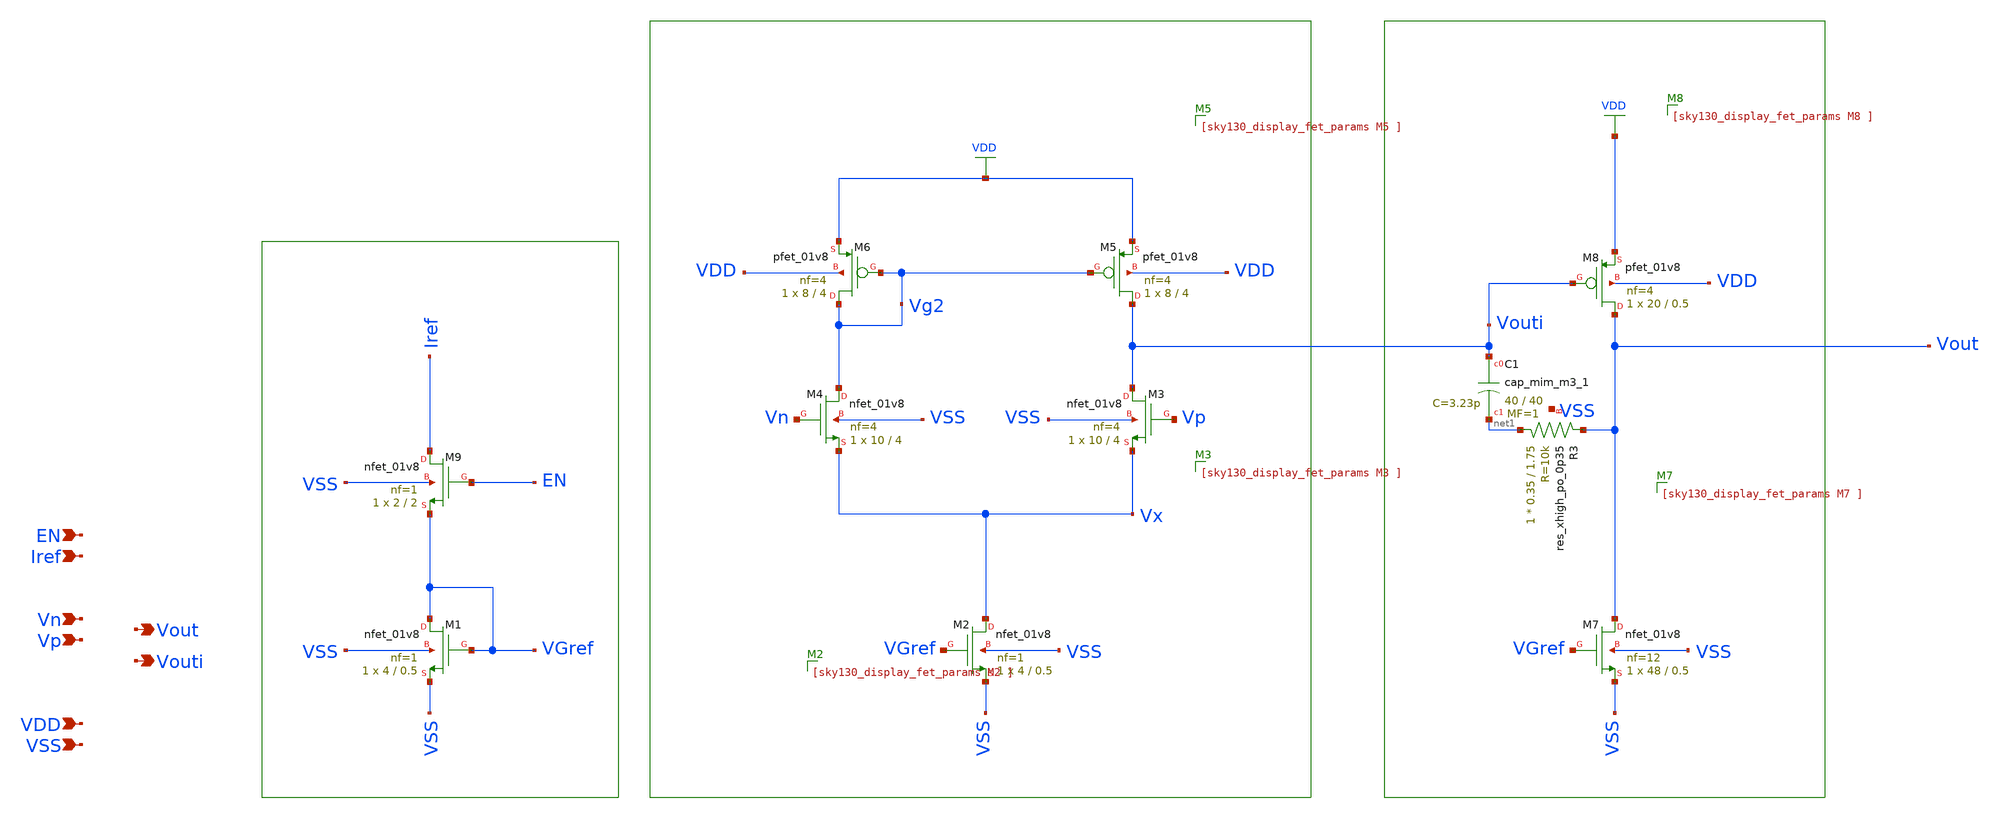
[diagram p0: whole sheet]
** sch_path: xschem/opamp.sch
**.subckt opamp VSS Vp Vout Vn VDD Iref Vouti EN
*.ipin VSS
*.ipin Vp
*.opin Vout
*.ipin Vn
*.ipin VDD
*.ipin Iref
*.opin Vouti
*.ipin EN
XM1 VGref VGref VSS VSS sky130_fd_pr__nfet_01v8 L=0.5 W=4 nf=1 ad='int((1 + 1)/2) * 4 / 1 * 0.29' as='int((1 + 2)/2) * 4 / 1 * 0.29'
+ pd='2*int((1 + 1)/2) * (4 / 1 + 0.29)' ps='2*int((1 + 2)/2) * (4 / 1 + 0.29)' nrd='0.29 / 4 ' nrs='0.29 / 4 '
+ sa=0 sb=0 sd=0 mult=1 m=1
XM2 Vx VGref VSS VSS sky130_fd_pr__nfet_01v8 L=0.5 W=4 nf=1 ad='int((1 + 1)/2) * 4 / 1 * 0.29' as='int((1 + 2)/2) * 4 / 1 * 0.29'
+ pd='2*int((1 + 1)/2) * (4 / 1 + 0.29)' ps='2*int((1 + 2)/2) * (4 / 1 + 0.29)' nrd='0.29 / 4 ' nrs='0.29 / 4 '
+ sa=0 sb=0 sd=0 mult=1 m=1
XM3 Vouti Vp Vx VSS sky130_fd_pr__nfet_01v8 L=4 W=10 nf=4 ad='int((4 + 1)/2) * 10 / 4 * 0.29' as='int((4 + 2)/2) * 10 / 4 * 0.29'
+ pd='2*int((4 + 1)/2) * (10 / 4 + 0.29)' ps='2*int((4 + 2)/2) * (10 / 4 + 0.29)' nrd='0.29 / 10 ' nrs='0.29 / 10 '
+ sa=0 sb=0 sd=0 mult=1 m=1
XM4 Vg2 Vn Vx VSS sky130_fd_pr__nfet_01v8 L=4 W=10 nf=4 ad='int((4 + 1)/2) * 10 / 4 * 0.29' as='int((4 + 2)/2) * 10 / 4 * 0.29'
+ pd='2*int((4 + 1)/2) * (10 / 4 + 0.29)' ps='2*int((4 + 2)/2) * (10 / 4 + 0.29)' nrd='0.29 / 10 ' nrs='0.29 / 10 '
+ sa=0 sb=0 sd=0 mult=1 m=1
XM5 Vouti Vg2 VDD VDD sky130_fd_pr__pfet_01v8 L=4 W=8 nf=4 ad='int((4 + 1)/2) * 8 / 4 * 0.29' as='int((4 + 2)/2) * 8 / 4 * 0.29'
+ pd='2*int((4 + 1)/2) * (8 / 4 + 0.29)' ps='2*int((4 + 2)/2) * (8 / 4 + 0.29)' nrd='0.29 / 8 ' nrs='0.29 / 8 '
+ sa=0 sb=0 sd=0 mult=1 m=1
XM6 Vg2 Vg2 VDD VDD sky130_fd_pr__pfet_01v8 L=4 W=8 nf=4 ad='int((4 + 1)/2) * 8 / 4 * 0.29' as='int((4 + 2)/2) * 8 / 4 * 0.29'
+ pd='2*int((4 + 1)/2) * (8 / 4 + 0.29)' ps='2*int((4 + 2)/2) * (8 / 4 + 0.29)' nrd='0.29 / 8 ' nrs='0.29 / 8 '
+ sa=0 sb=0 sd=0 mult=1 m=1
XM7 Vout VGref VSS VSS sky130_fd_pr__nfet_01v8 L=0.5 W=48 nf=12 ad='int((12 + 1)/2) * 48 / 12 * 0.29'
+ as='int((12 + 2)/2) * 48 / 12 * 0.29' pd='2*int((12 + 1)/2) * (48 / 12 + 0.29)' ps='2*int((12 + 2)/2) * (48 / 12 + 0.29)'
+ nrd='0.29 / 48 ' nrs='0.29 / 48 ' sa=0 sb=0 sd=0 mult=1 m=1
XM8 Vout Vouti VDD VDD sky130_fd_pr__pfet_01v8 L=0.5 W=20 nf=4 ad='int((4 + 1)/2) * 20 / 4 * 0.29' as='int((4 + 2)/2) * 20 / 4 * 0.29'
+ pd='2*int((4 + 1)/2) * (20 / 4 + 0.29)' ps='2*int((4 + 2)/2) * (20 / 4 + 0.29)' nrd='0.29 / 20 ' nrs='0.29 / 20 '
+ sa=0 sb=0 sd=0 mult=1 m=1
XM9 Iref EN VGref VSS sky130_fd_pr__nfet_01v8 L=2 W=2 nf=1 ad='int((1 + 1)/2) * 2 / 1 * 0.29' as='int((1 + 2)/2) * 2 / 1 * 0.29'
+ pd='2*int((1 + 1)/2) * (2 / 1 + 0.29)' ps='2*int((1 + 2)/2) * (2 / 1 + 0.29)' nrd='0.29 / 2 ' nrs='0.29 / 2 '
+ sa=0 sb=0 sd=0 mult=1 m=1
XC1 Vouti net1 sky130_fd_pr__cap_mim_m3_1 W=40 L=40 MF=1 m=1
XR3 net1 Vout VSS sky130_fd_pr__res_xhigh_po_0p35 L=1.75 mult=1 m=1
**.ends
.GLOBAL VDD
.end
